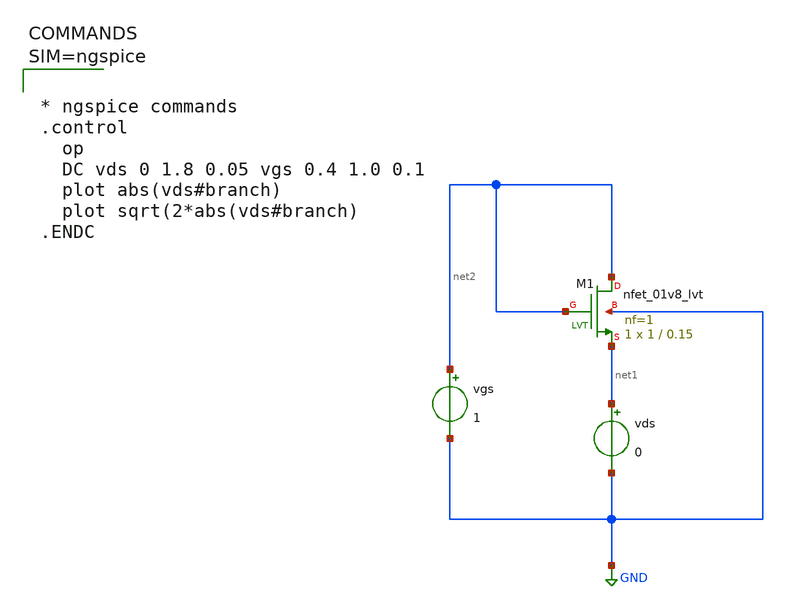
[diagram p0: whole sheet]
** sch_path: xschem/untitled-9.sch
**.subckt untitled-9
XM1 net2 net2 net1 GND sky130_fd_pr__nfet_01v8_lvt L=0.15 W=1 nf=1 ad='int((1 + 1)/2) * 1 / 1 * 0.29'
+ as='int((1 + 2)/2) * 1 / 1 * 0.29' pd='2*int((1 + 1)/2) * (1 / 1 + 0.29)' ps='2*int((1 + 2)/2) * (1 / 1 + 0.29)'
+ nrd='0.29 / 1 ' nrs='0.29 / 1 ' sa=0 sb=0 sd=0 mult=1 m=1
vgs net2 GND 1
vds net1 GND 0
**** begin user architecture code

** opencircuitdesign pdks install
.lib $::SKYWATER_MODELS/sky130.lib.spice tt




* ngspice commands
.control
  op
  DC vds 0 1.8 0.05 vgs 0.4 1.0 0.1
  plot abs(vds#branch)
  plot sqrt(2*abs(vds#branch)
.ENDC



**** end user architecture code
**.ends
.GLOBAL GND
.end
